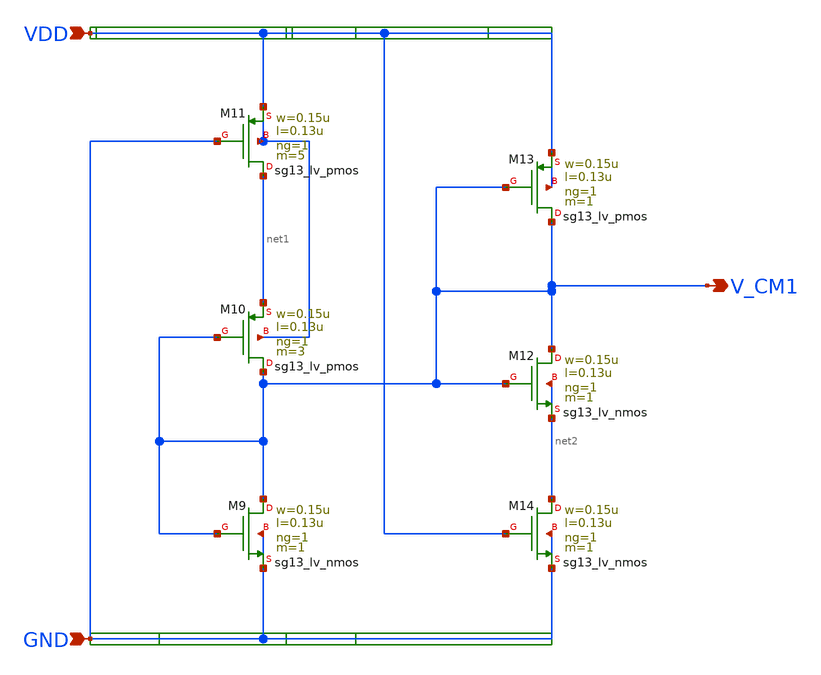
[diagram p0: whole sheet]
** sch_path: Design Files/RAMP/Fully-Diff-RAMP/STG1-CM.sch
**.subckt STG1-CM VDD GND V_CM1
*.ipin VDD
*.ipin GND
*.opin V_CM1
XM9 V_CM1 V_CM1 GND GND sg13_lv_nmos w=0.15u l=0.13u ng=1 m=1 mm_ok=1
XM10 V_CM1 V_CM1 net1 VDD sg13_lv_pmos w=0.15u l=0.13u ng=1 m=3 mm_ok=1
XM11 net1 GND VDD VDD sg13_lv_pmos w=0.15u l=0.13u ng=1 m=5 mm_ok=1
XM12 V_CM1 V_CM1 net2 net2 sg13_lv_nmos w=0.15u l=0.13u ng=1 m=1 mm_ok=1
XM13 V_CM1 V_CM1 VDD VDD sg13_lv_pmos w=0.15u l=0.13u ng=1 m=1 mm_ok=1
XM14 net2 VDD GND GND sg13_lv_nmos w=0.15u l=0.13u ng=1 m=1 mm_ok=1
**.ends
.end
